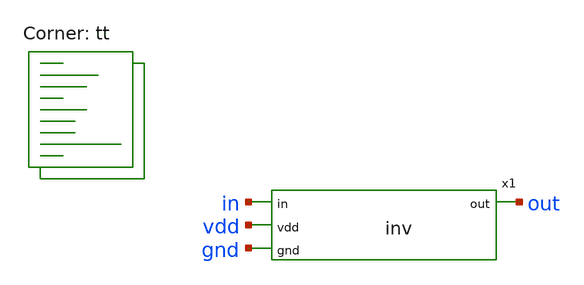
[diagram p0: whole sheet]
** sch_path: xschem/inv-tb.sch
**.subckt inv-tb
x1 in out vdd gnd inv
**** begin user architecture code



  .param max_freq=100e6 period={1/max_freq} time_high={period/2}
  .param delay_vin1={time_high} delay_vin2={time_high*1.5}
  .param lval=100u

  .option wnflag=1
  .option safecurrents

  Vdd vdd gnd 1.8
  Vref in gnd pulse(0 1.8 {delay_vin1} 1p 1p {time_high} {period})

  .control
     reset
     save all
     tran 0.1n 3u
     write inv-tb.raw
     set appendwrite

     reset
     save all
     dc vref 0 1.8 0.1
     write inv-tb.raw
*    quit 0
  .endc



.lib $::SKYWATER_MODELS/sky130.lib.spice tt
**** end user architecture code
**.ends

* expanding   symbol:  inv.sym # of pins=4
** sym_path: xschem/inv.sym
** sch_path: xschem/inv.sch
.subckt inv in out vdd gnd
*.ipin in
*.opin out
*.ipin vdd
*.ipin gnd
XM1 out in gnd gnd sky130_fd_pr__nfet_01v8 L=0.15 W=0.42 nf=1 ad='int((nf+1)/2) * W/nf * 0.29' as='int((nf+2)/2) * W/nf * 0.29'
+ pd='2*int((nf+1)/2) * (W/nf + 0.29)' ps='2*int((nf+2)/2) * (W/nf + 0.29)' nrd='0.29 / W' nrs='0.29 / W'
+ sa=0 sb=0 sd=0 mult=1 m=1
XM2 out in vdd vdd sky130_fd_pr__pfet_01v8 L=0.15 W=1.26 nf=1 ad='int((nf+1)/2) * W/nf * 0.29' as='int((nf+2)/2) * W/nf * 0.29'
+ pd='2*int((nf+1)/2) * (W/nf + 0.29)' ps='2*int((nf+2)/2) * (W/nf + 0.29)' nrd='0.29 / W' nrs='0.29 / W'
+ sa=0 sb=0 sd=0 mult=1 m=1
.ends

.end
